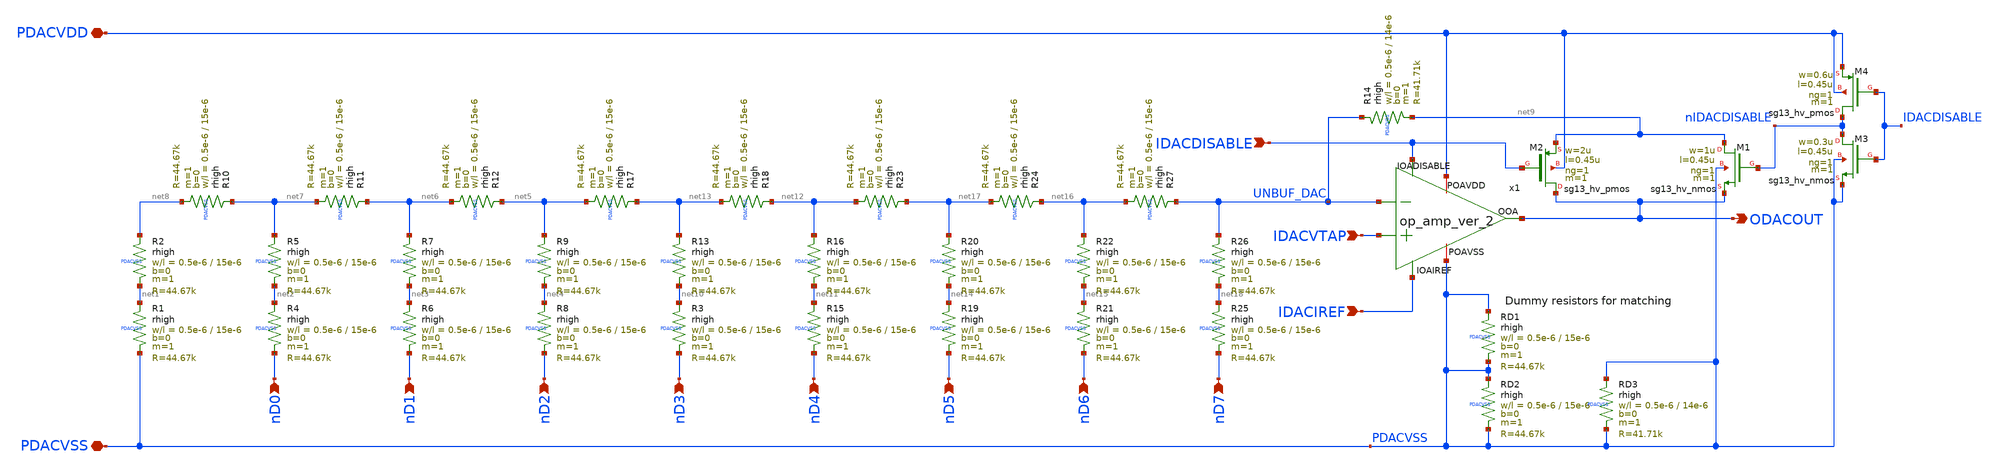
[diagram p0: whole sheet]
** sch_path: macros/heichips26_analog_project/macros/r2r_dac/schematic/xschem/r2r_dac.sch
**.subckt r2r_dac PDACVDD PDACVSS nD0 nD1 nD2 IDACIREF ODACOUT nD3 nD4 nD5 nD6 nD7 IDACVTAP
*+ IDACDISABLE
*.iopin PDACVDD
*.iopin PDACVSS
*.ipin nD0
*.ipin nD1
*.ipin nD2
*.ipin IDACIREF
*.opin ODACOUT
*.ipin nD3
*.ipin nD4
*.ipin nD5
*.ipin nD6
*.ipin nD7
*.ipin IDACVTAP
*.ipin IDACDISABLE
XR1 net1 PDACVSS PDACVSS rhigh w=0.5e-6 l=15e-6 m=1 b=0 mm_ok=1
XR2 net8 net1 PDACVSS rhigh w=0.5e-6 l=15e-6 m=1 b=0 mm_ok=1
XR4 net2 nD0 PDACVSS rhigh w=0.5e-6 l=15e-6 m=1 b=0 mm_ok=1
XR5 net7 net2 PDACVSS rhigh w=0.5e-6 l=15e-6 m=1 b=0 mm_ok=1
XR6 net3 nD1 PDACVSS rhigh w=0.5e-6 l=15e-6 m=1 b=0 mm_ok=1
XR7 net6 net3 PDACVSS rhigh w=0.5e-6 l=15e-6 m=1 b=0 mm_ok=1
XR8 net4 nD2 PDACVSS rhigh w=0.5e-6 l=15e-6 m=1 b=0 mm_ok=1
XR9 net5 net4 PDACVSS rhigh w=0.5e-6 l=15e-6 m=1 b=0 mm_ok=1
XR10 net7 net8 PDACVSS rhigh w=0.5e-6 l=15e-6 m=1 b=0 mm_ok=1
XR11 net6 net7 PDACVSS rhigh w=0.5e-6 l=15e-6 m=1 b=0 mm_ok=1
XR12 net5 net6 PDACVSS rhigh w=0.5e-6 l=15e-6 m=1 b=0 mm_ok=1
XR14 UNBUF_DAC net9 PDACVSS rhigh w=0.5e-6 l=14e-6 m=1 b=0 mm_ok=1
XR3 net10 nD3 PDACVSS rhigh w=0.5e-6 l=15e-6 m=1 b=0 mm_ok=1
XR13 net13 net10 PDACVSS rhigh w=0.5e-6 l=15e-6 m=1 b=0 mm_ok=1
XR15 net11 nD4 PDACVSS rhigh w=0.5e-6 l=15e-6 m=1 b=0 mm_ok=1
XR16 net12 net11 PDACVSS rhigh w=0.5e-6 l=15e-6 m=1 b=0 mm_ok=1
XR17 net13 net5 PDACVSS rhigh w=0.5e-6 l=15e-6 m=1 b=0 mm_ok=1
XR18 net12 net13 PDACVSS rhigh w=0.5e-6 l=15e-6 m=1 b=0 mm_ok=1
XR19 net14 nD5 PDACVSS rhigh w=0.5e-6 l=15e-6 m=1 b=0 mm_ok=1
XR20 net17 net14 PDACVSS rhigh w=0.5e-6 l=15e-6 m=1 b=0 mm_ok=1
XR21 net15 nD6 PDACVSS rhigh w=0.5e-6 l=15e-6 m=1 b=0 mm_ok=1
XR22 net16 net15 PDACVSS rhigh w=0.5e-6 l=15e-6 m=1 b=0 mm_ok=1
XR23 net17 net12 PDACVSS rhigh w=0.5e-6 l=15e-6 m=1 b=0 mm_ok=1
XR24 net16 net17 PDACVSS rhigh w=0.5e-6 l=15e-6 m=1 b=0 mm_ok=1
XR25 net18 nD7 PDACVSS rhigh w=0.5e-6 l=15e-6 m=1 b=0 mm_ok=1
XR26 UNBUF_DAC net18 PDACVSS rhigh w=0.5e-6 l=15e-6 m=1 b=0 mm_ok=1
XR27 UNBUF_DAC net16 PDACVSS rhigh w=0.5e-6 l=15e-6 m=1 b=0 mm_ok=1
x1 PDACVDD IDACIREF UNBUF_DAC ODACOUT IDACVTAP PDACVSS IDACDISABLE op_amp_ver_2
XM1 net9 nIDACDISABLE ODACOUT PDACVSS sg13_hv_nmos w=1u l=0.45u ng=1 m=1 mm_ok=1
XM2 ODACOUT IDACDISABLE net9 PDACVDD sg13_hv_pmos w=2u l=0.45u ng=1 m=1 mm_ok=1
XRD2 PDACVSS PDACVSS PDACVSS rhigh w=0.5e-6 l=15e-6 m=1 b=0 mm_ok=1
XRD1 PDACVSS PDACVSS PDACVSS rhigh w=0.5e-6 l=15e-6 m=1 b=0 mm_ok=1
XRD3 PDACVSS PDACVSS PDACVSS rhigh w=0.5e-6 l=14e-6 m=1 b=0 mm_ok=1
XM3 nIDACDISABLE IDACDISABLE PDACVSS PDACVSS sg13_hv_nmos w=0.3u l=0.45u ng=1 m=1 mm_ok=1
XM4 nIDACDISABLE IDACDISABLE PDACVDD PDACVDD sg13_hv_pmos w=0.6u l=0.45u ng=1 m=1 mm_ok=1
**.ends
.end
